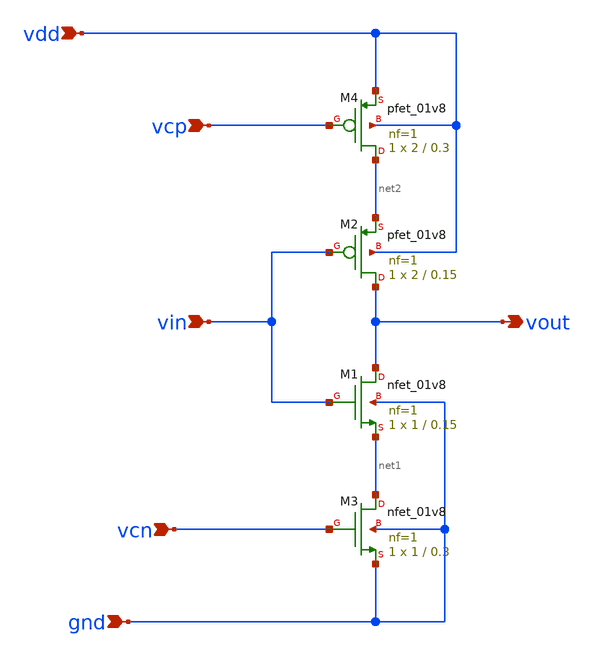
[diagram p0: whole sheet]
** sch_path: xsch/cstarve_stage.sch
**.subckt cstarve_stage vdd gnd vcp vcn vin vout
*.ipin vdd
*.ipin gnd
*.ipin vcp
*.ipin vcn
*.ipin vin
*.opin vout
XM1 vout vin net1 gnd sky130_fd_pr__nfet_01v8 L=0.15 W=1 nf=1 ad='int((nf+1)/2) * W/nf * 0.29' as='int((nf+2)/2) * W/nf * 0.29'
+ pd='2*int((nf+1)/2) * (W/nf + 0.29)' ps='2*int((nf+2)/2) * (W/nf + 0.29)' nrd='0.29 / W' nrs='0.29 / W'
+ sa=0 sb=0 sd=0 mult=1 m=1
XM2 vout vin net2 vdd sky130_fd_pr__pfet_01v8 L=0.15 W=2 nf=1 ad='int((nf+1)/2) * W/nf * 0.29' as='int((nf+2)/2) * W/nf * 0.29'
+ pd='2*int((nf+1)/2) * (W/nf + 0.29)' ps='2*int((nf+2)/2) * (W/nf + 0.29)' nrd='0.29 / W' nrs='0.29 / W'
+ sa=0 sb=0 sd=0 mult=1 m=1
XM3 net1 vcn gnd gnd sky130_fd_pr__nfet_01v8 L=0.3 W=1 nf=1 ad='int((nf+1)/2) * W/nf * 0.29' as='int((nf+2)/2) * W/nf * 0.29'
+ pd='2*int((nf+1)/2) * (W/nf + 0.29)' ps='2*int((nf+2)/2) * (W/nf + 0.29)' nrd='0.29 / W' nrs='0.29 / W'
+ sa=0 sb=0 sd=0 mult=1 m=1
XM4 net2 vcp vdd vdd sky130_fd_pr__pfet_01v8 L=0.3 W=2 nf=1 ad='int((nf+1)/2) * W/nf * 0.29' as='int((nf+2)/2) * W/nf * 0.29'
+ pd='2*int((nf+1)/2) * (W/nf + 0.29)' ps='2*int((nf+2)/2) * (W/nf + 0.29)' nrd='0.29 / W' nrs='0.29 / W'
+ sa=0 sb=0 sd=0 mult=1 m=1
**.ends
.end
